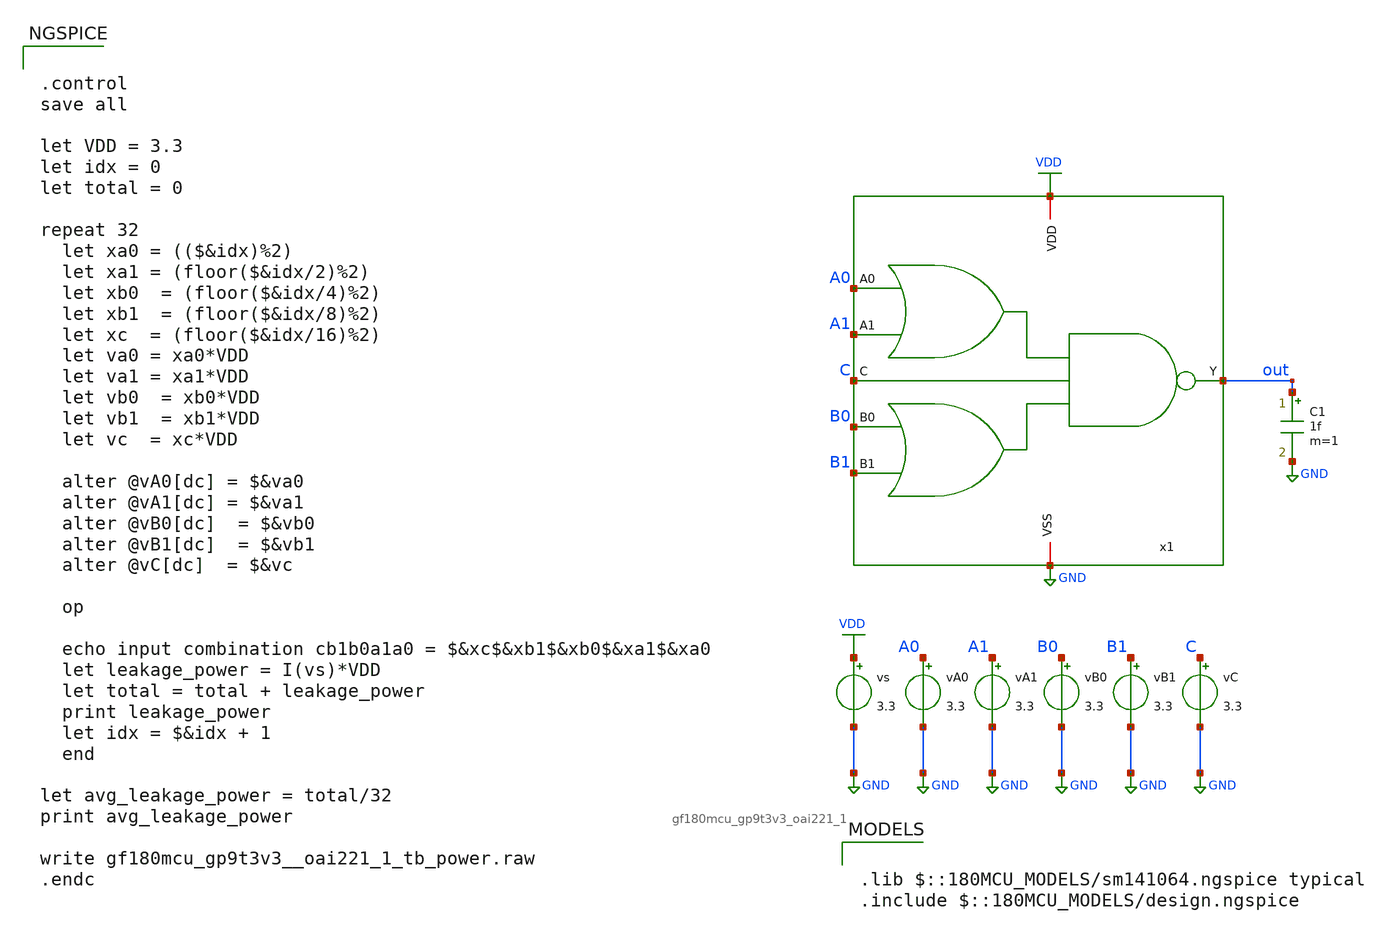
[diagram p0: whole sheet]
** sch_path: designs/oai221/gf180mcu_gp9t3v3_oai221_1_tb_power.sch
**.subckt gf180mcu_gp9t3v3_oai221_1_tb_power
vA0 A0 GND 3.3
vs VDD GND 3.3
vA1 A1 GND 3.3
vB1 B1 GND 3.3
vB0 B0 GND 3.3
vC C GND 3.3
C1 out GND 1f m=1
x1 VDD A0 B0 C A1 B1 out GND gf180mcu_gp9t3v3_oai221_1
**** begin user architecture code


.control
save all

let VDD = 3.3
let idx = 0
let total = 0

repeat 32
  let xa0 = (($&idx)%2)
  let xa1 = (floor($&idx/2)%2)
  let xb0  = (floor($&idx/4)%2)
  let xb1  = (floor($&idx/8)%2)
  let xc  = (floor($&idx/16)%2)
  let va0 = xa0*VDD
  let va1 = xa1*VDD
  let vb0  = xb0*VDD
  let vb1  = xb1*VDD
  let vc  = xc*VDD

  alter @vA0[dc] = $&va0
  alter @vA1[dc] = $&va1
  alter @vB0[dc]  = $&vb0
  alter @vB1[dc]  = $&vb1
  alter @vC[dc]  = $&vc

  op

  echo input combination cb1b0a1a0 = $&xc$&xb1$&xb0$&xa1$&xa0
  let leakage_power = I(vs)*VDD
  let total = total + leakage_power
  print leakage_power
  let idx = $&idx + 1
  end

let avg_leakage_power = total/32
print avg_leakage_power

write gf180mcu_gp9t3v3__oai221_1_tb_power.raw
.endc



.lib $::180MCU_MODELS/sm141064.ngspice typical
.include $::180MCU_MODELS/design.ngspice

**** end user architecture code
**.ends
.GLOBAL VDD
.GLOBAL GND
.end
